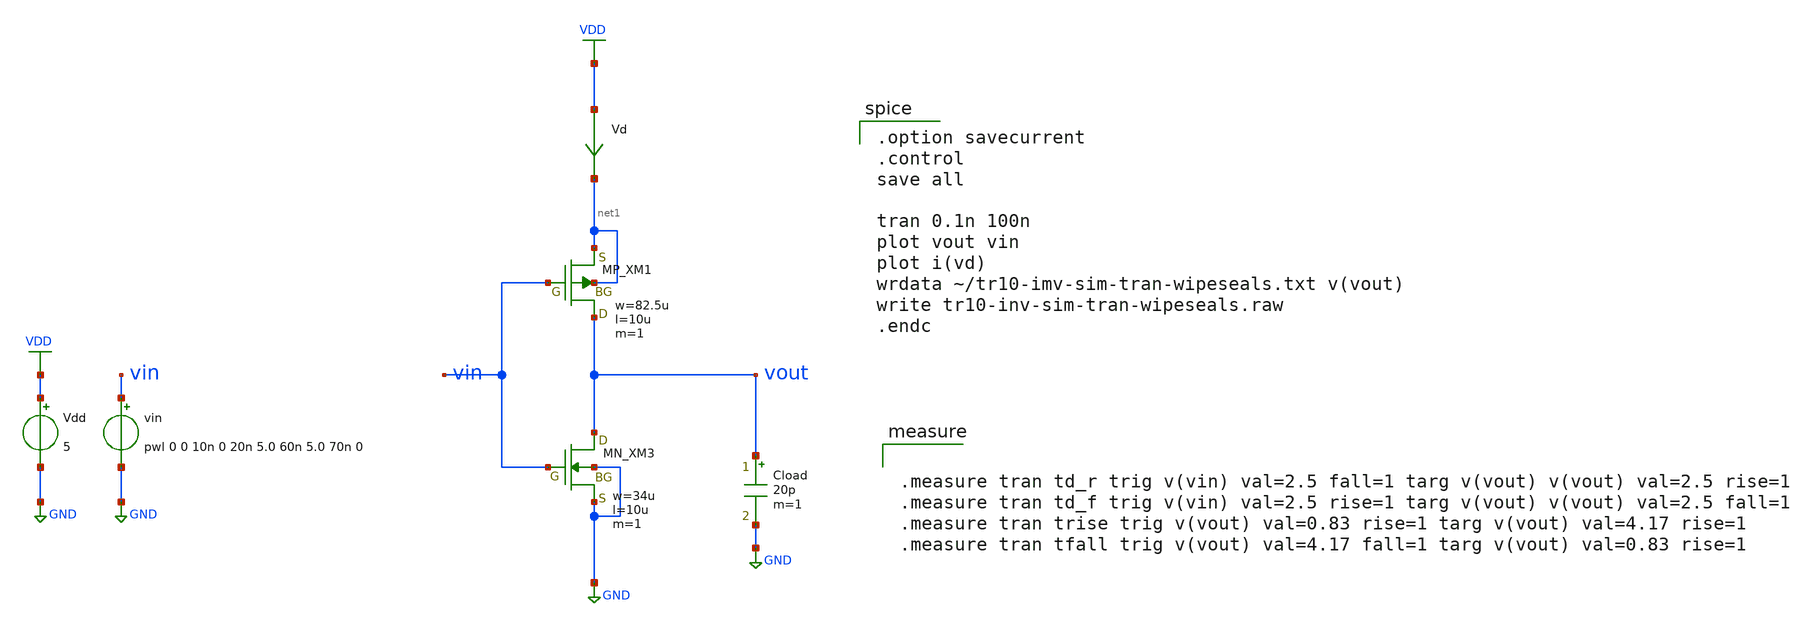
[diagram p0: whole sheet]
** sch_path: member_project/inverter/wipeseals/misc/tr10-inv-sim-cload20p-wipeseals.sch
**.subckt tr10-inv-sim-cload20p-wipeseals
Vdd VDD GND 5
Vd VDD net1 0
.save i(vd)
Cload vout GND 20p m=1
XM1 vout vin net1 net1 PMOS w=82.5u l=10u as=0 ad=0 ps=0 pd=0 nrd=0 nrs=0 m=1
XM3 vout vin GND GND NMOS w=34u l=10u as=0 ad=0 ps=0 pd=0 nrd=0 nrs=0 m=1
vin vin GND pwl 0 0 10n 0 20n 5.0 60n 5.0 70n 0
**** begin user architecture code
 .include $::LIB/../ip62_models


.measure tran td_r trig v(vin) val=2.5 fall=1 targ v(vout) v(vout) val=2.5 rise=1
.measure tran td_f trig v(vin) val=2.5 rise=1 targ v(vout) v(vout) val=2.5 fall=1
.measure tran trise trig v(vout) val=0.83 rise=1 targ v(vout) val=4.17 rise=1
.measure tran tfall trig v(vout) val=4.17 fall=1 targ v(vout) val=0.83 rise=1



.option savecurrent
.control
save all

tran 0.1n 100n
plot vout vin
plot i(vd)
wrdata ~/tr10-imv-sim-tran-wipeseals.txt v(vout)
write tr10-inv-sim-tran-wipeseals.raw
.endc


**** end user architecture code
**.ends
.GLOBAL VDD
.GLOBAL GND
.end
